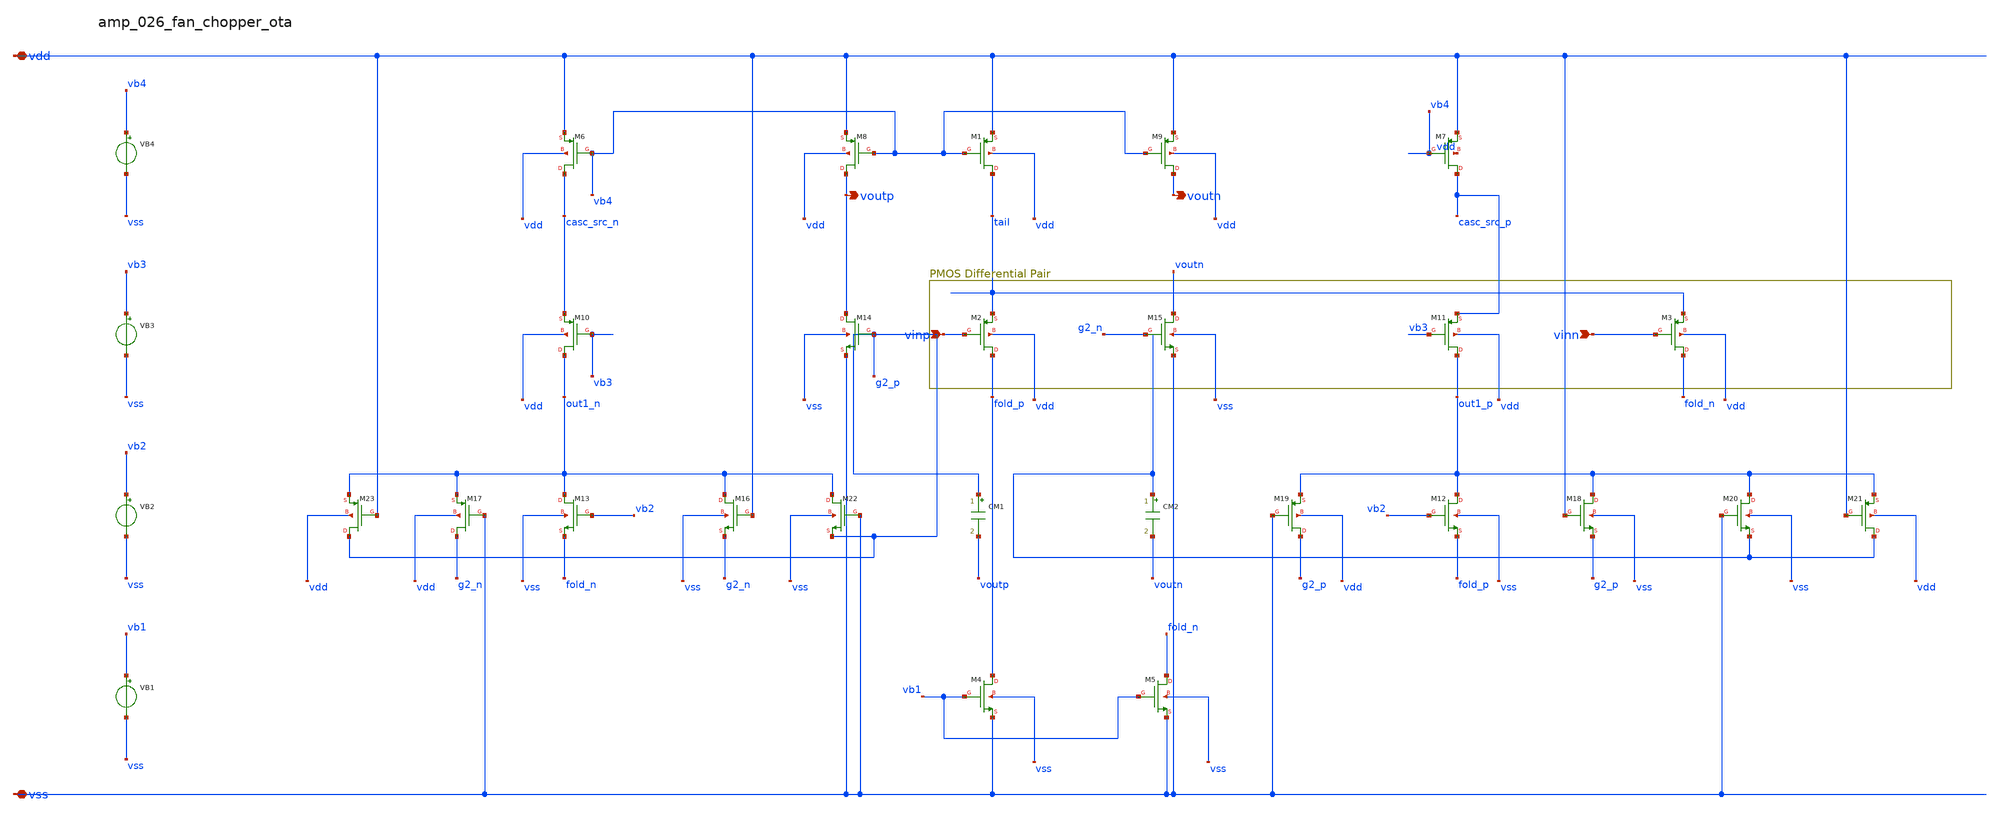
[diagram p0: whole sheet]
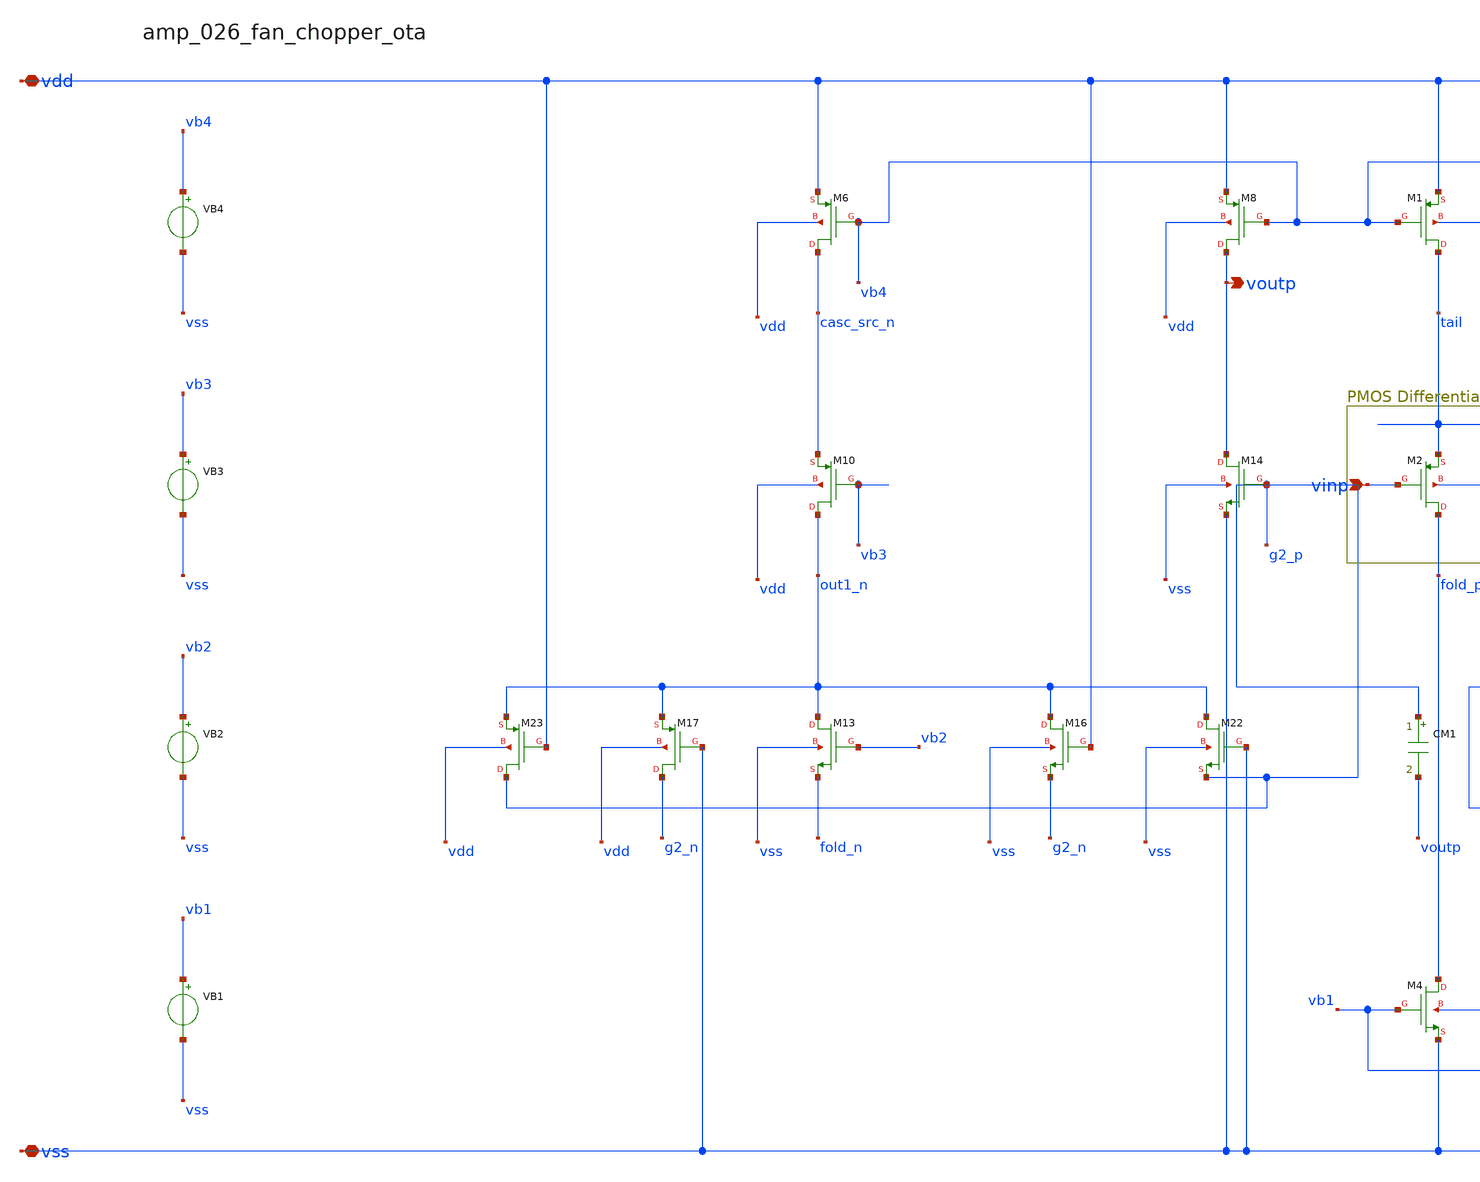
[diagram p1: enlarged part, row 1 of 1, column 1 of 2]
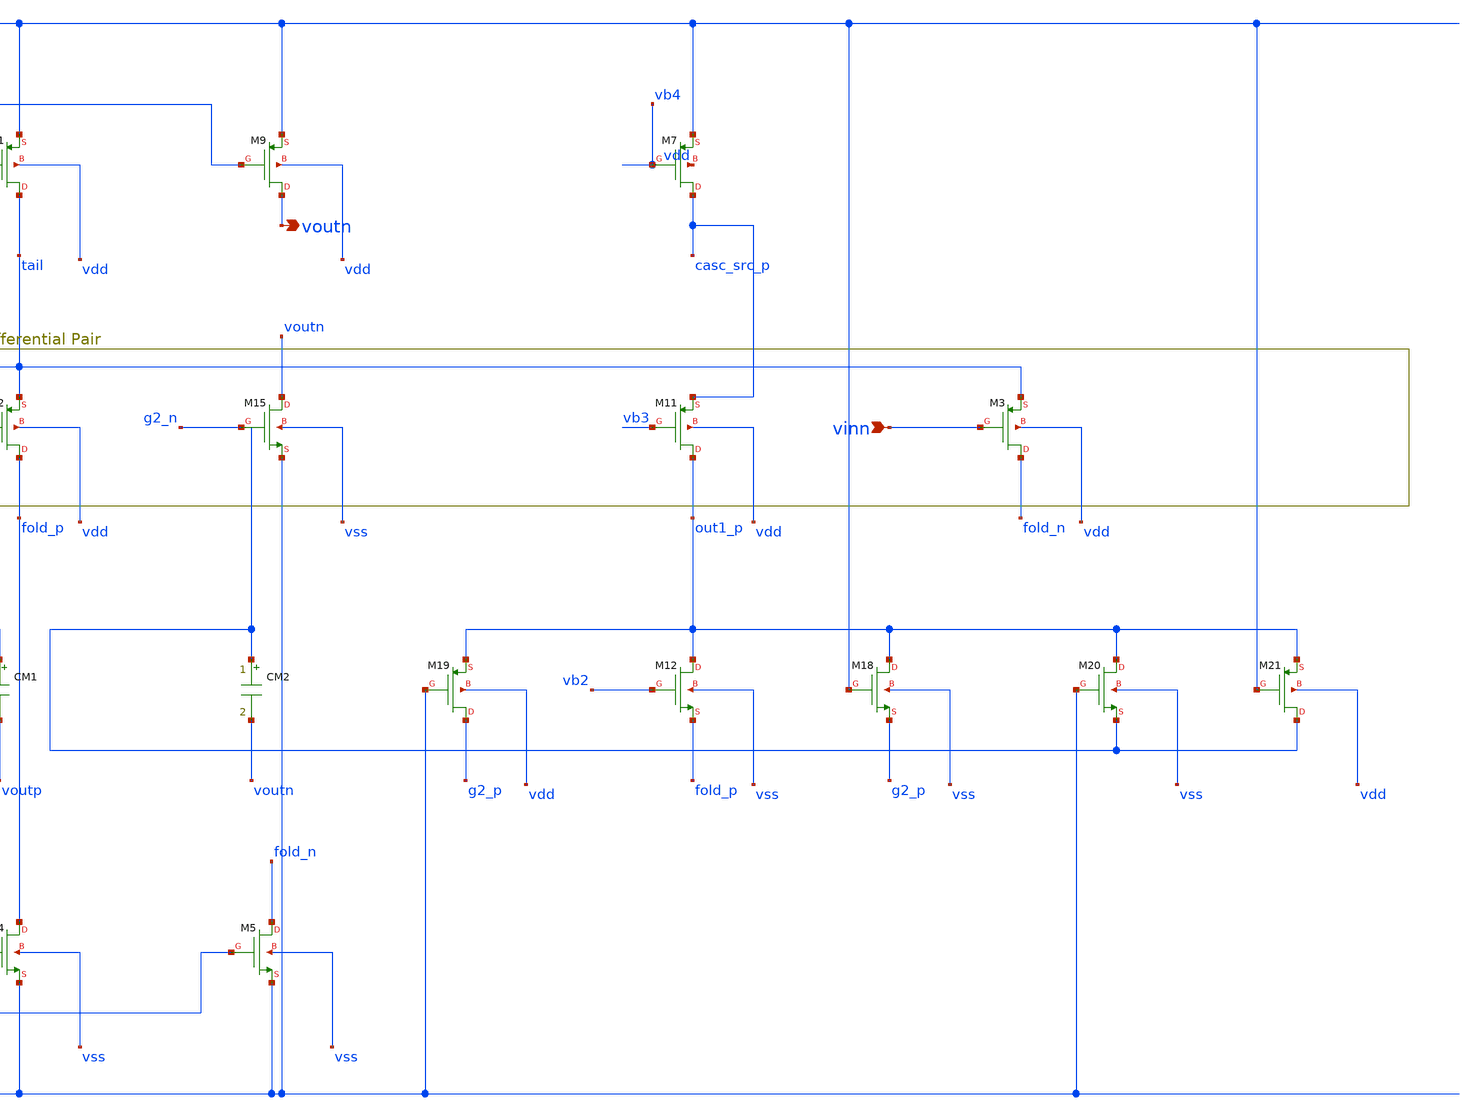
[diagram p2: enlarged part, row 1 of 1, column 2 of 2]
** sch_path: analog-db/raw/amp_026_fan_chopper_ota/amp_026_fan_chopper_ota_annotated.sch
**.subckt amp_026_fan_chopper_ota_annotated vinp vinn vdd vss voutp voutn
*.ipin vinp
*.ipin vinn
*.iopin vdd
*.iopin vss
*.opin voutp
*.opin voutn
CM1 g2_p voutp 'x_dut_cm1_value' m=1
CM2 g2_n voutn 'x_dut_cm2_value' m=1
VB1 vb1 vss dc {vb1}
VB2 vb2 vss dc {vb2}
VB3 vb3 vss dc {vb3}
VB4 vb4 vss dc {vb4}
XM1 tail vb4 vdd vdd sg13_lv_pmos w=x_dut_xm1_w l=x_dut_xm1_l ng=1 m=x_dut_xm1_m
XM10 out1_n vb3 casc_src_n vdd sg13_lv_pmos w=x_dut_xm10_w l=x_dut_xm10_l ng=1 m=x_dut_xm10_m
XM11 out1_p vb3 casc_src_p vdd sg13_lv_pmos w=x_dut_xm11_w l=x_dut_xm11_l ng=1 m=x_dut_xm11_m
XM12 out1_p vb2 fold_p vss sg13_lv_nmos w=x_dut_xm12_w l=x_dut_xm12_l ng=1 m=x_dut_xm12_m
XM13 out1_n vb2 fold_n vss sg13_lv_nmos w=x_dut_xm13_w l=x_dut_xm13_l ng=1 m=x_dut_xm13_m
XM14 voutp g2_p vss vss sg13_lv_nmos w=x_dut_xm14_w l=x_dut_xm14_l ng=1 m=x_dut_xm14_m
XM15 voutn g2_n vss vss sg13_lv_nmos w=x_dut_xm15_w l=x_dut_xm15_l ng=1 m=x_dut_xm15_m
XM16 out1_n vdd g2_n vss sg13_lv_nmos w=x_dut_xm16_w l=x_dut_xm16_l ng=1 m=x_dut_xm16_m
XM17 g2_n vss out1_n vdd sg13_lv_pmos w=x_dut_xm17_w l=x_dut_xm17_l ng=1 m=x_dut_xm17_m
XM18 out1_p vdd g2_p vss sg13_lv_nmos w=x_dut_xm18_w l=x_dut_xm18_l ng=1 m=x_dut_xm18_m
XM19 g2_p vss out1_p vdd sg13_lv_pmos w=x_dut_xm19_w l=x_dut_xm19_l ng=1 m=x_dut_xm19_m
XM2 fold_p vinp tail vdd sg13_lv_pmos w=x_dut_xm2_w l=x_dut_xm2_l ng=1 m=x_dut_xm2_m
XM20 out1_p vss g2_n vss sg13_lv_nmos w=x_dut_xm20_w l=x_dut_xm20_l ng=1 m=x_dut_xm20_m
XM21 g2_n vdd out1_p vdd sg13_lv_pmos w=x_dut_xm21_w l=x_dut_xm21_l ng=1 m=x_dut_xm21_m
XM22 out1_n vss g2_p vss sg13_lv_nmos w=x_dut_xm22_w l=x_dut_xm22_l ng=1 m=x_dut_xm22_m
XM23 g2_p vdd out1_n vdd sg13_lv_pmos w=x_dut_xm23_w l=x_dut_xm23_l ng=1 m=x_dut_xm23_m
XM3 fold_n vinn tail vdd sg13_lv_pmos w=x_dut_xm3_w l=x_dut_xm3_l ng=1 m=x_dut_xm3_m
XM4 fold_p vb1 vss vss sg13_lv_nmos w=x_dut_xm4_w l=x_dut_xm4_l ng=1 m=x_dut_xm4_m
XM5 fold_n vb1 vss vss sg13_lv_nmos w=x_dut_xm5_w l=x_dut_xm5_l ng=1 m=x_dut_xm5_m
XM6 casc_src_n vb4 vdd vdd sg13_lv_pmos w=x_dut_xm6_w l=x_dut_xm6_l ng=1 m=x_dut_xm6_m
XM7 casc_src_p vb4 vdd vdd sg13_lv_pmos w=x_dut_xm7_w l=x_dut_xm7_l ng=1 m=x_dut_xm7_m
XM8 voutp vb4 vdd vdd sg13_lv_pmos w=x_dut_xm8_w l=x_dut_xm8_l ng=1 m=x_dut_xm8_m
XM9 voutn vb4 vdd vdd sg13_lv_pmos w=x_dut_xm9_w l=x_dut_xm9_l ng=1 m=x_dut_xm9_m
**.ends
.end
